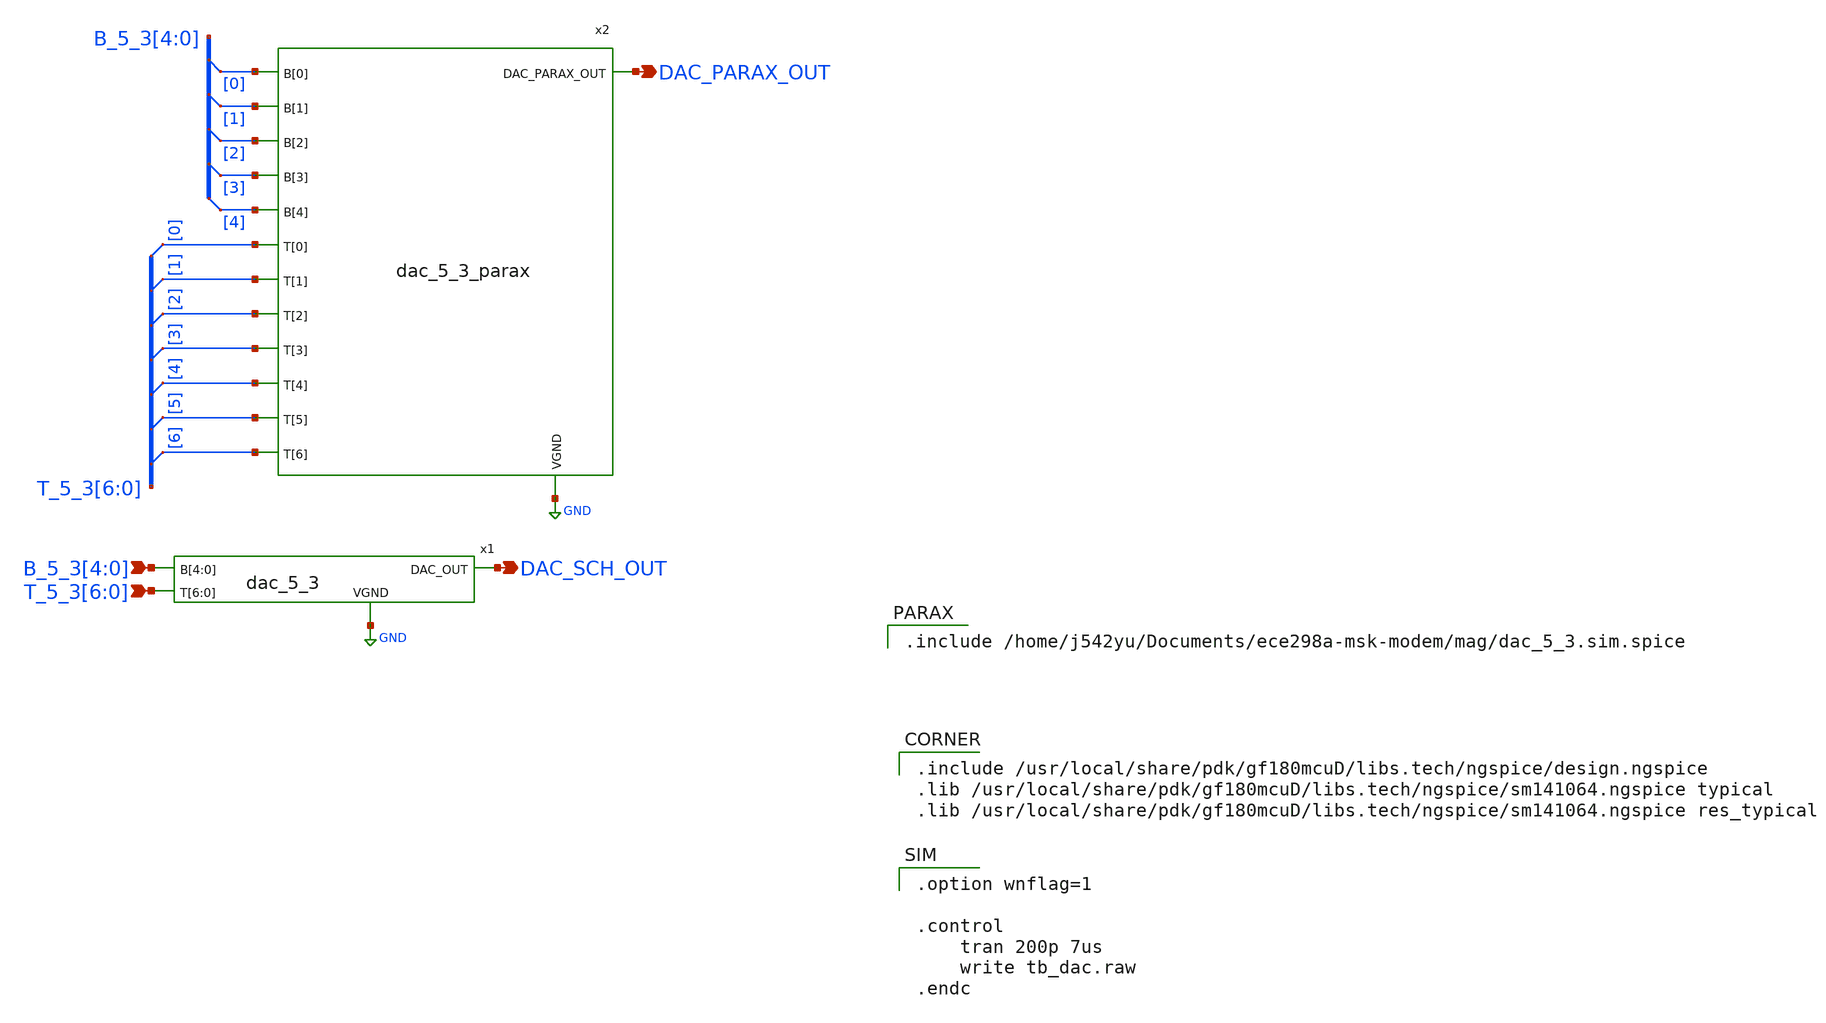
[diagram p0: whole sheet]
** sch_path: xschem/tb_dac.sch
**.subckt tb_dac B_5_3[4],B_5_3[3],B_5_3[2],B_5_3[1],B_5_3[0]
*+ T_5_3[6],T_5_3[5],T_5_3[4],T_5_3[3],T_5_3[2],T_5_3[1],T_5_3[0] DAC_SCH_OUT DAC_PARAX_OUT
*.ipin B_5_3[4],B_5_3[3],B_5_3[2],B_5_3[1],B_5_3[0]
*.ipin T_5_3[6],T_5_3[5],T_5_3[4],T_5_3[3],T_5_3[2],T_5_3[1],T_5_3[0]
*.opin DAC_SCH_OUT
*.opin DAC_PARAX_OUT
x1 DAC_SCH_OUT B_5_3[4] B_5_3[3] B_5_3[2] B_5_3[1] B_5_3[0] T_5_3[6] T_5_3[5] T_5_3[4] T_5_3[3]
+ T_5_3[2] T_5_3[1] T_5_3[0] GND dac_5_3
x2 B_5_3[0] B_5_3[1] B_5_3[2] B_5_3[3] B_5_3[4] T_5_3[0] T_5_3[1] T_5_3[2] T_5_3[3] T_5_3[4]
+ T_5_3[5] T_5_3[6] DAC_PARAX_OUT GND dac_5_3_parax
* tap: B_5_3[4:0] --> B_5_3[0]
* tap: B_5_3[4:0] --> B_5_3[1]
* tap: B_5_3[4:0] --> B_5_3[2]
* tap: B_5_3[4:0] --> B_5_3[3]
* tap: B_5_3[4:0] --> B_5_3[4]
* tap: T_5_3[6:0] --> T_5_3[0]
* tap: T_5_3[6:0] --> T_5_3[1]
* tap: T_5_3[6:0] --> T_5_3[2]
* tap: T_5_3[6:0] --> T_5_3[3]
* tap: T_5_3[6:0] --> T_5_3[4]
* tap: T_5_3[6:0] --> T_5_3[5]
* tap: T_5_3[6:0] --> T_5_3[6]
**** begin user architecture code

.option wnflag=1

.control
    tran 200p 7us
    write tb_dac.raw
.endc



.include /home/j542yu/Documents/ece298a-msk-modem/xschem/simulation/dac_ramp_sampling-50.0MHz_3.3V_5_3.spice


.include /usr/local/share/pdk/gf180mcuD/libs.tech/ngspice/design.ngspice
.lib /usr/local/share/pdk/gf180mcuD/libs.tech/ngspice/sm141064.ngspice typical
.lib /usr/local/share/pdk/gf180mcuD/libs.tech/ngspice/sm141064.ngspice res_typical


.include /home/j542yu/Documents/ece298a-msk-modem/mag/dac_5_3.sim.spice

**** end user architecture code
**.ends

* expanding   symbol:  dac_5_3.sym # of pins=4
** sym_path: xschem/dac_5_3.sym
** sch_path: xschem/dac_5_3.sch
.subckt dac_5_3 DAC_OUT B[4] B[3] B[2] B[1] B[0] T[6] T[5] T[4] T[3] T[2] T[1] T[0] VGND
*.ipin B[4],B[3],B[2],B[1],B[0]
*.ipin T[6],T[5],T[4],T[3],T[2],T[1],T[0]
*.opin DAC_OUT
*.iopin VGND
x1 net2 net1 B[0] VGND dac_sub_r2r
x2 net3 net2 B[1] VGND dac_sub_r2r
x3 net4 net3 B[2] VGND dac_sub_r2r
x4 net5 net4 B[3] VGND dac_sub_r2r
x5 DAC_OUT net5 B[4] VGND dac_sub_r2r
* tap: B[4:0] --> B[0]
* tap: B[4:0] --> B[1]
* tap: B[4:0] --> B[2]
* tap: B[4:0] --> B[3]
* tap: B[4:0] --> B[4]
x6 DAC_OUT T[0] VGND dac_sub_therm
x7 DAC_OUT T[1] VGND dac_sub_therm
x8 DAC_OUT T[2] VGND dac_sub_therm
x9 DAC_OUT T[3] VGND dac_sub_therm
x10 DAC_OUT T[4] VGND dac_sub_therm
x11 DAC_OUT T[5] VGND dac_sub_therm
x12 DAC_OUT T[6] VGND dac_sub_therm
* tap: T[6:0] --> T[0]
* tap: T[6:0] --> T[1]
* tap: T[6:0] --> T[2]
* tap: T[6:0] --> T[3]
* tap: T[6:0] --> T[4]
* tap: T[6:0] --> T[5]
* tap: T[6:0] --> T[6]
XR2 VGND net6 VGND ppolyf_u_1k r_width=2e-6 r_length=20e-6 m=1
XR3 net6 net1 VGND ppolyf_u_1k r_width=2e-6 r_length=20e-6 m=1
XR4 VGND VGND VGND ppolyf_u_1k r_width=2e-6 r_length=20e-6 m=1
XR5 VGND VGND VGND ppolyf_u_1k r_width=2e-6 r_length=20e-6 m=1
XR7 VGND VGND VGND ppolyf_u_1k r_width=2e-6 r_length=20e-6 m=1
.ends


* expanding   symbol:  dac_5_3_parax.sym # of pins=14
** sym_path: xschem/dac_5_3_parax.sym
.include /home/j542yu/Documents/ece298a-msk-modem/mag/dac_5_3.sim.spice

* expanding   symbol:  dac_sub_r2r.sym # of pins=4
** sym_path: xschem/dac_sub_r2r.sym
** sch_path: xschem/dac_sub_r2r.sch
.subckt dac_sub_r2r R_node_out R_node_in in VGND
*.ipin in
*.iopin R_node_out
*.iopin R_node_in
*.iopin VGND
XR7 in net1 VGND ppolyf_u_1k r_width=2e-6 r_length=20e-6 m=1
XR1 net1 R_node_in VGND ppolyf_u_1k r_width=2e-6 r_length=20e-6 m=1
XR2 net2 R_node_in VGND ppolyf_u_1k r_width=2e-6 r_length=20e-6 m=1
XR3 R_node_out net2 VGND ppolyf_u_1k r_width=2e-6 r_length=20e-6 m=1
XR4 net3 R_node_in VGND ppolyf_u_1k r_width=2e-6 r_length=20e-6 m=1
XR5 R_node_out net3 VGND ppolyf_u_1k r_width=2e-6 r_length=20e-6 m=1
.ends


* expanding   symbol:  dac_sub_therm.sym # of pins=3
** sym_path: xschem/dac_sub_therm.sym
** sch_path: xschem/dac_sub_therm.sch
.subckt dac_sub_therm R_node in VGND
*.ipin in
*.iopin R_node
*.iopin VGND
XR7 in net1 VGND ppolyf_u_1k r_width=2e-6 r_length=20e-6 m=1
XR1 net1 R_node VGND ppolyf_u_1k r_width=2e-6 r_length=20e-6 m=1
.ends

.GLOBAL GND
.end
